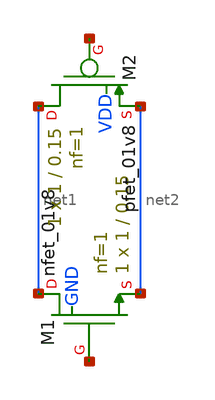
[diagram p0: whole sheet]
** sch_path: xschem/untitled.sch
**.subckt untitled
XM1 net1 net3 net2 GND sky130_fd_pr__nfet_01v8 L=0.15 W=1 nf=1 ad='int((nf+1)/2) * W/nf * 0.29' as='int((nf+2)/2) * W/nf * 0.29'
+ pd='2*int((nf+1)/2) * (W/nf + 0.29)' ps='2*int((nf+2)/2) * (W/nf + 0.29)' nrd='0.29 / W' nrs='0.29 / W'
+ sa=0 sb=0 sd=0 mult=1 m=1
XM2 net1 net4 net2 VDD sky130_fd_pr__pfet_01v8 L=0.15 W=1 nf=1 ad='int((nf+1)/2) * W/nf * 0.29' as='int((nf+2)/2) * W/nf * 0.29'
+ pd='2*int((nf+1)/2) * (W/nf + 0.29)' ps='2*int((nf+2)/2) * (W/nf + 0.29)' nrd='0.29 / W' nrs='0.29 / W'
+ sa=0 sb=0 sd=0 mult=1 m=1
**.ends
.end
